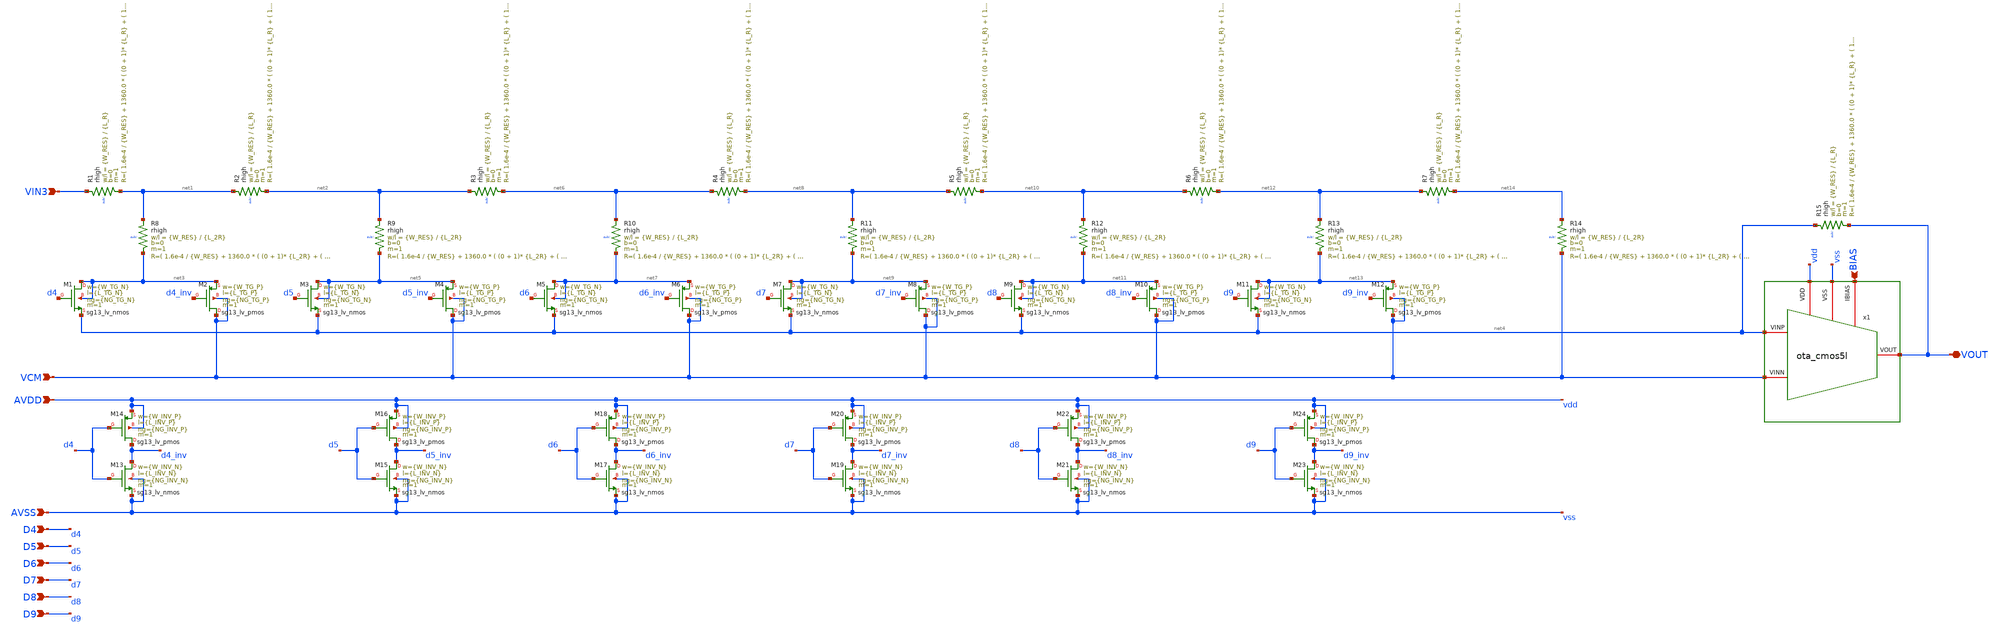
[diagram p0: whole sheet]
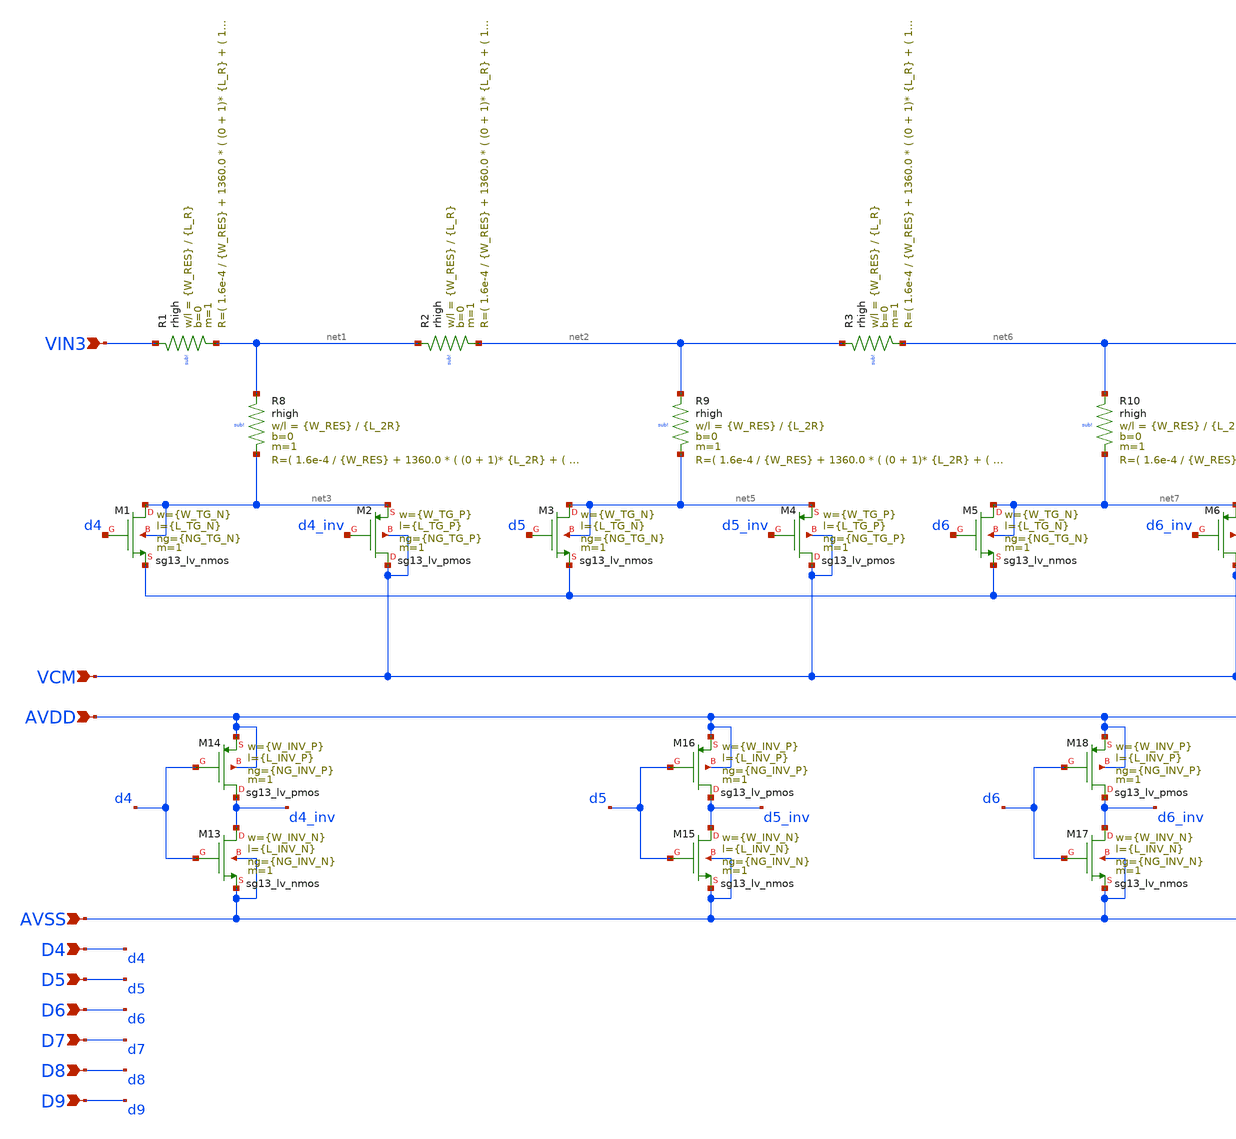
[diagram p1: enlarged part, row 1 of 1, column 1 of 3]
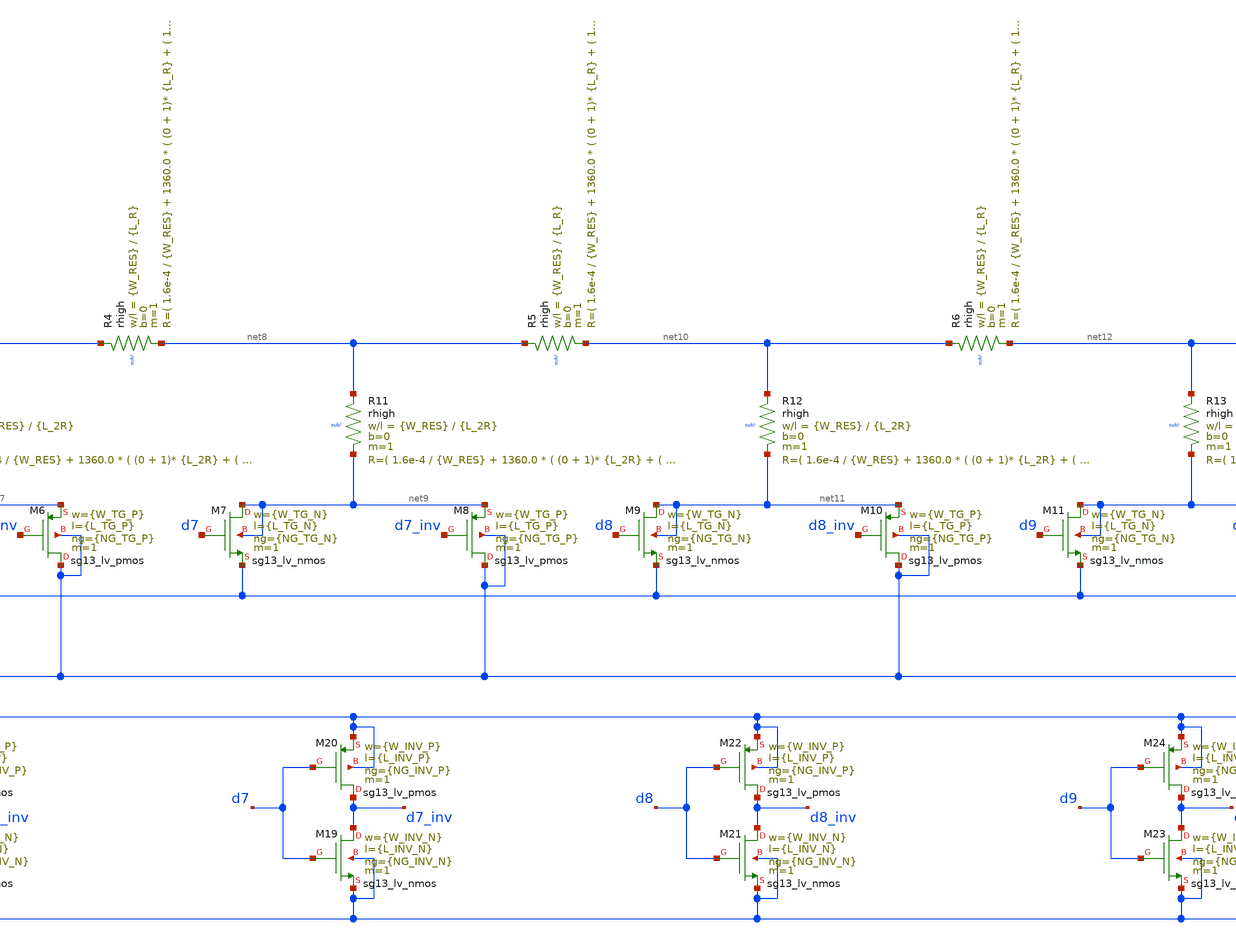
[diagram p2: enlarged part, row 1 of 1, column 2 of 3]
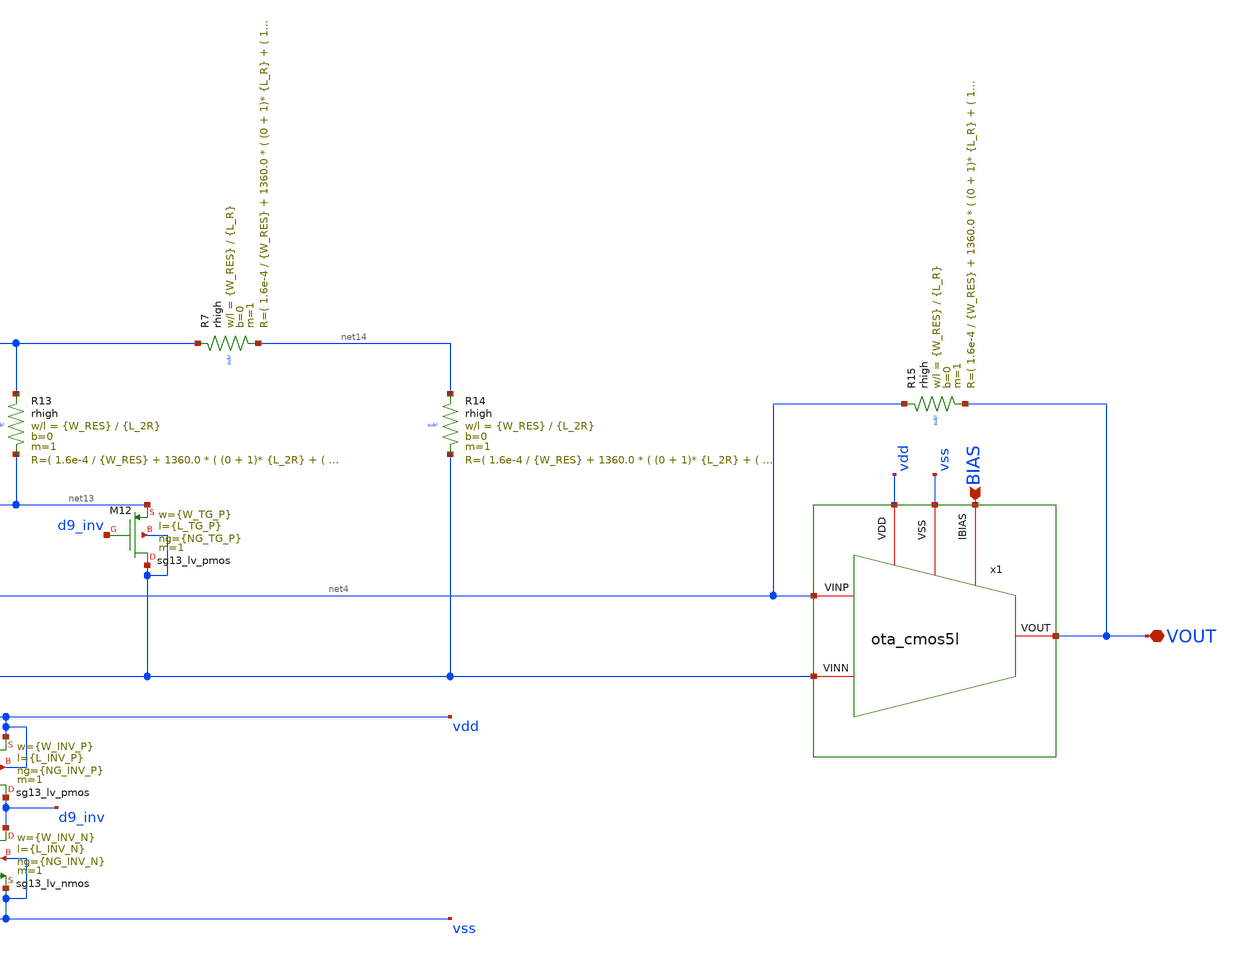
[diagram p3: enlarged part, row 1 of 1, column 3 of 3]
** sch_path: designs/libs/core_analog/fine_gain/fine_gain.sch
**.subckt fine_gain VIN3 VCM D4 D5 D6 D7 D8 D9 BIAS VOUT AVDD AVSS
*.ipin VIN3
*.ipin VCM
*.ipin D4
*.ipin D5
*.ipin D6
*.ipin D7
*.ipin D8
*.ipin D9
*.ipin BIAS
*.iopin VOUT
*.ipin AVDD
*.ipin AVSS
XR1 VIN3 net1 sub! rhigh w={W_RES} l={L_R} m=1 b=0 mm_ok=1
XM1 net3 d4 net4 net3 sg13_lv_nmos w={W_TG_N} l={L_TG_N} ng={NG_TG_N} m=1 mm_ok=1
XM2 VCM d4_inv net3 VCM sg13_lv_pmos w={W_TG_P} l={L_TG_P} ng={NG_TG_P} m=1 mm_ok=1
x1 vss BIAS vdd VCM net4 VOUT ota_cmos5l
XR2 net1 net2 sub! rhigh w={W_RES} l={L_R} m=1 b=0 mm_ok=1
XR8 net1 net3 sub! rhigh w={W_RES} l={L_2R} m=1 b=0 mm_ok=1
XR9 net2 net5 sub! rhigh w={W_RES} l={L_2R} m=1 b=0 mm_ok=1
XR15 net4 VOUT sub! rhigh w={W_RES} l={L_R} m=1 b=0 mm_ok=1
XM3 net5 d5 net4 net5 sg13_lv_nmos w={W_TG_N} l={L_TG_N} ng={NG_TG_N} m=1 mm_ok=1
XM4 VCM d5_inv net5 VCM sg13_lv_pmos w={W_TG_P} l={L_TG_P} ng={NG_TG_P} m=1 mm_ok=1
XR3 net2 net6 sub! rhigh w={W_RES} l={L_R} m=1 b=0 mm_ok=1
XR4 net6 net8 sub! rhigh w={W_RES} l={L_R} m=1 b=0 mm_ok=1
XR5 net8 net10 sub! rhigh w={W_RES} l={L_R} m=1 b=0 mm_ok=1
XR6 net10 net12 sub! rhigh w={W_RES} l={L_R} m=1 b=0 mm_ok=1
XR7 net12 net14 sub! rhigh w={W_RES} l={L_R} m=1 b=0 mm_ok=1
XR10 net6 net7 sub! rhigh w={W_RES} l={L_2R} m=1 b=0 mm_ok=1
XM5 net7 d6 net4 net7 sg13_lv_nmos w={W_TG_N} l={L_TG_N} ng={NG_TG_N} m=1 mm_ok=1
XM6 VCM d6_inv net7 VCM sg13_lv_pmos w={W_TG_P} l={L_TG_P} ng={NG_TG_P} m=1 mm_ok=1
XR11 net8 net9 sub! rhigh w={W_RES} l={L_2R} m=1 b=0 mm_ok=1
XM7 net9 d7 net4 net9 sg13_lv_nmos w={W_TG_N} l={L_TG_N} ng={NG_TG_N} m=1 mm_ok=1
XM8 VCM d7_inv net9 VCM sg13_lv_pmos w={W_TG_P} l={L_TG_P} ng={NG_TG_P} m=1 mm_ok=1
XR12 net10 net11 sub! rhigh w={W_RES} l={L_2R} m=1 b=0 mm_ok=1
XM9 net11 d8 net4 net11 sg13_lv_nmos w={W_TG_N} l={L_TG_N} ng={NG_TG_N} m=1 mm_ok=1
XM10 VCM d8_inv net11 VCM sg13_lv_pmos w={W_TG_P} l={L_TG_P} ng={NG_TG_P} m=1 mm_ok=1
XR13 net12 net13 sub! rhigh w={W_RES} l={L_2R} m=1 b=0 mm_ok=1
XM11 net13 d9 net4 net13 sg13_lv_nmos w={W_TG_N} l={L_TG_N} ng={NG_TG_N} m=1 mm_ok=1
XM12 VCM d9_inv net13 VCM sg13_lv_pmos w={W_TG_P} l={L_TG_P} ng={NG_TG_P} m=1 mm_ok=1
XR14 net14 VCM sub! rhigh w={W_RES} l={L_2R} m=1 b=0 mm_ok=1
XM13 d4_inv d4 AVSS AVSS sg13_lv_nmos w={W_INV_N} l={L_INV_N} ng={NG_INV_N} m=1 mm_ok=1
XM14 d4_inv d4 AVDD AVDD sg13_lv_pmos w={W_INV_P} l={L_INV_P} ng={NG_INV_P} m=1 mm_ok=1
XM15 d5_inv d5 AVSS AVSS sg13_lv_nmos w={W_INV_N} l={L_INV_N} ng={NG_INV_N} m=1 mm_ok=1
XM16 d5_inv d5 AVDD AVDD sg13_lv_pmos w={W_INV_P} l={L_INV_P} ng={NG_INV_P} m=1 mm_ok=1
XM17 d6_inv d6 AVSS AVSS sg13_lv_nmos w={W_INV_N} l={L_INV_N} ng={NG_INV_N} m=1 mm_ok=1
XM18 d6_inv d6 AVDD AVDD sg13_lv_pmos w={W_INV_P} l={L_INV_P} ng={NG_INV_P} m=1 mm_ok=1
XM19 d7_inv d7 AVSS AVSS sg13_lv_nmos w={W_INV_N} l={L_INV_N} ng={NG_INV_N} m=1 mm_ok=1
XM20 d7_inv d7 AVDD AVDD sg13_lv_pmos w={W_INV_P} l={L_INV_P} ng={NG_INV_P} m=1 mm_ok=1
XM21 d8_inv d8 AVSS AVSS sg13_lv_nmos w={W_INV_N} l={L_INV_N} ng={NG_INV_N} m=1 mm_ok=1
XM22 d8_inv d8 AVDD AVDD sg13_lv_pmos w={W_INV_P} l={L_INV_P} ng={NG_INV_P} m=1 mm_ok=1
XM23 d9_inv d9 AVSS AVSS sg13_lv_nmos w={W_INV_N} l={L_INV_N} ng={NG_INV_N} m=1 mm_ok=1
XM24 d9_inv d9 AVDD AVDD sg13_lv_pmos w={W_INV_P} l={L_INV_P} ng={NG_INV_P} m=1 mm_ok=1
**.ends

* expanding   symbol:
*+  /foss/designs/chipalooza/Programmable-Instrumentation-Amplifier-IP/designs/libs/core_analog/ota_cmos5l/ota_cmos5l.sym # of pins=6
** sym_path: /foss/designs/chipalooza/Programmable-Instrumentation-Amplifier-IP/designs/libs/core_analog/ota_cmos5l/ota_cmos5l.sym
** sch_path: /foss/designs/chipalooza/Programmable-Instrumentation-Amplifier-IP/designs/libs/core_analog/ota_cmos5l/ota_cmos5l.sch
.subckt ota_cmos5l VSS IBIAS VDD VINN VINP VOUT
*.iopin IBIAS
*.iopin VDD
*.iopin VSS
*.iopin VOUT
*.iopin VINP
*.iopin VINN
XM6 net1 net1 vdd vdd sg13_lv_pmos w={wbias} l={lbias} ng=1 m={m6} mm_ok=1
XM7 net5 net1 vdd vdd sg13_lv_pmos w={wbias} l={lbias} ng=1 m={m7} mm_ok=1
XM8 net6 net1 vdd vdd sg13_lv_pmos w={wbias} l={lbias} ng=1 m={m8} mm_ok=1
XM1 net7 VINN net2 vdd sg13_lv_pmos w={winpair} l={linpair} ng=1 m=1 mm_ok=1
XM2 net8 VINP net2 vdd sg13_lv_pmos w={winpair} l={linpair} ng=1 m=1 mm_ok=1
XM3 net3 net3 gnd gnd sg13_lv_nmos w={wload} l={lload} ng=1 m=1 mm_ok=1
XM4 net4 net3 gnd gnd sg13_lv_nmos w={wload} l={lload} ng=1 m=1 mm_ok=1
XM5 net9 net4 gnd gnd sg13_lv_nmos w={wcs} l={lcs} ng=1 m=1 mm_ok=1
C1 net10 net9 {Cc} m=1
XR1 net4 net10 sub! rhigh w=0.5e-6 l=1.95e-6 m=1 b=0 mm_ok=1
**** begin user architecture code



.include ota_cmos5l.save
.param temp=27
.param lbias=0.15u wbias=0.15u
.param m6=1 m7=4 m8=10
.param linpair=3u winpair=20u
.param lload=0.5u wload=0.42u
.param lcs=5u wcs=19.13u
.param Cc=1.5p
.control
op
write ota_cmos5l.raw
.endc



**** end user architecture code
**** begin user architecture code



.lib cornerMOSlv.lib mos_tt
.lib cornerMOShv.lib mos_tt
.lib cornerRES.lib res_typ
.lib cornerDIO.lib dio_tt



**** end user architecture code
VIBIAS net1 ibias 0
.save i(vibias)
VID7 net5 net2 0
.save i(vid7)
VID8 net6 VOUT 0
.save i(vid8)
VIVDD VDD vdd 0
.save i(vivdd)
.save v(vinp)
.save v(vinn)
.save v(vout)
VID1 net7 net3 0
.save i(vid1)
VID2 net8 net4 0
.save i(vid2)
VID5 VOUT net9 0
.save i(vid5)
.ends

.GLOBAL VDD
.end
